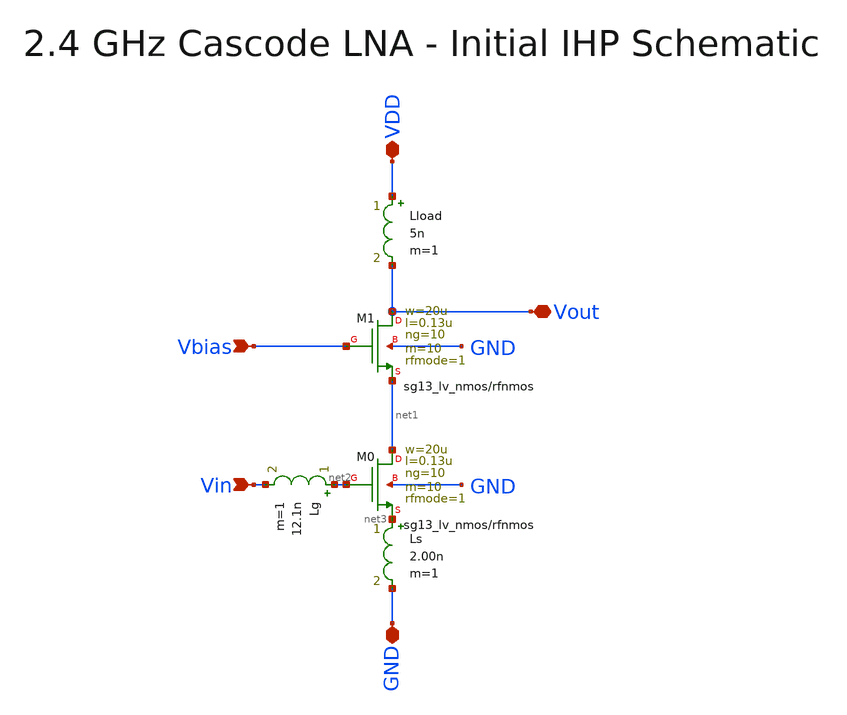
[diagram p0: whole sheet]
** sch_path: macros/lna/schematic/xschem/lna.sch
**.subckt lna VDD Vin Vbias Vout GND
*.iopin VDD
*.ipin Vin
*.ipin Vbias
*.iopin Vout
*.iopin GND
Lload VDD Vout 5n m=1
Lg net2 Vin 12.1n m=1
Ls net3 GND 2.00n m=1
XM0 net1 net2 net3 GND sg13_lv_nmos w=20u l=0.13u ng=10 m=10 rfmode=1 mm_ok=1
XM1 Vout Vbias net1 GND sg13_lv_nmos w=20u l=0.13u ng=10 m=10 rfmode=1 mm_ok=1
**.ends
.end
